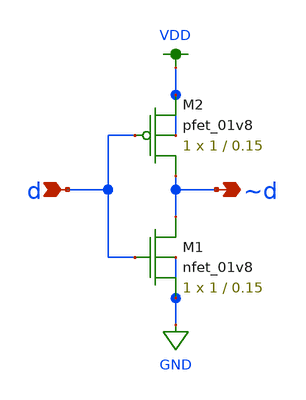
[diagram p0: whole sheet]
** sch_path: mini_proj_2/schematic/inverter.sch
**.subckt inverter d ~d
*.ipin d
*.opin ~d
XM1 ~d d GND GND sky130_fd_pr__nfet_01v8 L=0.15 W=1 nf=1 ad='int((nf+1)/2) * W/nf * 0.29' as='int((nf+2)/2) * W/nf * 0.29'
+ pd='2*int((nf+1)/2) * (W/nf + 0.29)' ps='2*int((nf+2)/2) * (W/nf + 0.29)' nrd='0.29 / W' nrs='0.29 / W'
+ sa=0 sb=0 sd=0 mult=1 m=1
XM2 ~d d VDD VDD sky130_fd_pr__pfet_01v8 L=0.15 W=1 nf=1 ad='int((nf+1)/2) * W/nf * 0.29' as='int((nf+2)/2) * W/nf * 0.29'
+ pd='2*int((nf+1)/2) * (W/nf + 0.29)' ps='2*int((nf+2)/2) * (W/nf + 0.29)' nrd='0.29 / W' nrs='0.29 / W'
+ sa=0 sb=0 sd=0 mult=1 m=1
**.ends
.GLOBAL VDD
.GLOBAL GND
.end
